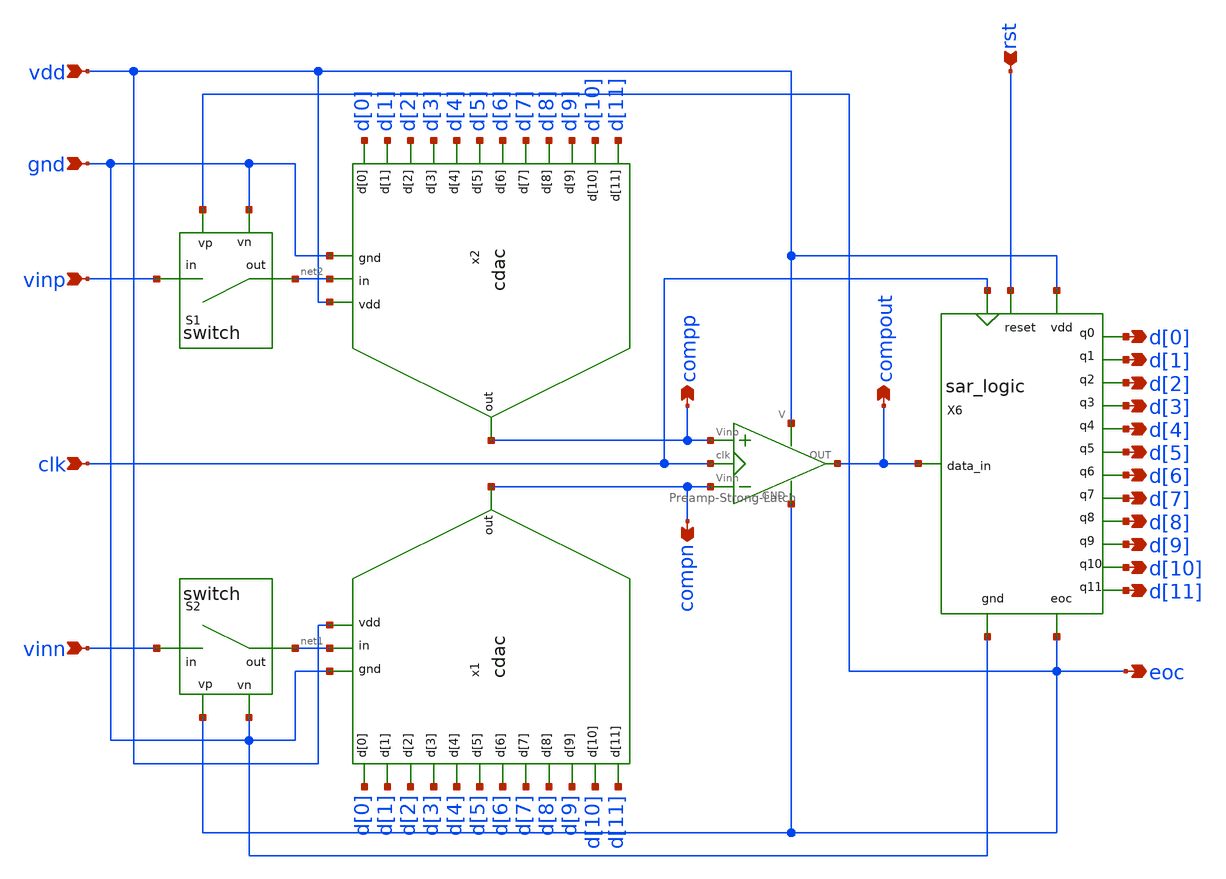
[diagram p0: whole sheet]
** sch_path: SAR_ADC/xschem/designs/sar_adc.sch
**.subckt sar_adc vinn vinp clk rst vdd gnd d[0] d[1] d[2] d[3] d[4] d[5] d[6] d[7] d[8] d[9] d[10]
*+ d[11] compp compn compout eoc
*.ipin vinn
*.ipin vinp
*.ipin clk
*.ipin rst
*.ipin vdd
*.ipin gnd
*.opin d[0]
*.opin d[1]
*.opin d[2]
*.opin d[3]
*.opin d[4]
*.opin d[5]
*.opin d[6]
*.opin d[7]
*.opin d[8]
*.opin d[9]
*.opin d[10]
*.opin d[11]
*.opin compp
*.opin compn
*.opin compout
*.opin eoc
x1 compn net1 d[9] d[7] d[0] d[11] d[3] d[4] d[2] d[1] d[8] d[6] d[5] d[10] gnd vdd cdac cu=5u
x2 compp net2 d[9] d[7] d[0] d[11] d[3] d[4] d[2] d[1] d[8] d[6] d[5] d[10] gnd vdd cdac cu=5u
X5 vdd compp compn compout clk eoc Preamp-Strong-Latch
X6 eoc vdd gnd clk compout d[0] d[10] d[11] d[1] d[2] d[3] d[4] d[5] d[6] d[7] d[8] d[9] rst
+ sar_logic
S1 vinp net2 eoc gnd swm1
S2 vinn net1 eoc gnd swm1
**.ends

* expanding   symbol:  cdac.sym # of pins=16
** sym_path: SAR_ADC/xschem/designs/cdac.sym
** sch_path: SAR_ADC/xschem/designs/cdac.sch
.subckt cdac out in d[9] d[7] d[0] d[11] d[3] d[4] d[2] d[1] d[8] d[6] d[5] d[10] gnd vdd  cu=5u
*.ipin d[0]
*.ipin d[1]
*.ipin d[2]
*.ipin d[3]
*.ipin d[4]
*.ipin d[5]
*.ipin d[6]
*.ipin d[7]
*.ipin d[8]
*.ipin d[9]
*.ipin d[10]
*.ipin d[11]
*.ipin vdd
*.ipin gnd
*.iopin out
*.iopin in
x1 in vdd gnd d[0] cdac_line CW={sqrt(2)*cu} CL={sqrt(2)*cu}
x2 in vdd gnd d[1] cdac_line CW={sqrt(3)*cu} CL={sqrt(3)*cu}
x3 in vdd gnd d[2] cdac_line CW={sqrt(4)*cu} CL={sqrt(4)*cu}
x4 in vdd gnd d[3] cdac_line CW={sqrt(8)*cu} CL={sqrt(8)*cu}
x5 in vdd gnd d[4] cdac_line CW={sqrt(16)*cu} CL={sqrt(16)*cu}
x6 in vdd gnd d[5] cdac_line CW={sqrt(32)*cu} CL={sqrt(32)*cu}
XCA out in cap_mim_1f5fF c_width={cu} c_length={cu} m=1
x7 out vdd gnd d[6] cdac_line CW={sqrt(1)*cu} CL={sqrt(1)*cu}
x8 out vdd gnd d[7] cdac_line CW={sqrt(2)*cu} CL={sqrt(2)*cu}
x9 out vdd gnd d[8] cdac_line CW={sqrt(4)*cu} CL={sqrt(4)*cu}
x10 out vdd gnd d[9] cdac_line CW={sqrt(8)*cu} CL={sqrt(8)*cu}
x11 out vdd gnd d[10] cdac_line CW={sqrt(16)*cu} CL={sqrt(16)*cu}
x12 out vdd gnd d[11] cdac_line CW={sqrt(32)*cu} CL={sqrt(32)*cu}
R1 out in 100T m=1
XC1 in gnd cap_mim_1f5fF c_width={cu} c_length={cu} m=1
.ends


* expanding   symbol:  Preamp-Strong-Latch.sym # of pins=6
** sym_path: SAR_ADC/xschem/designs/Preamp-Strong-Latch.sym
** sch_path: SAR_ADC/xschem/designs/Preamp-Strong-Latch.sch
.subckt Preamp-Strong-Latch V Vinp Vinn OUT clk GND
*.iopin V
*.iopin GND
*.iopin Vinp
*.iopin Vinn
*.iopin clk
*.iopin OUT
X1 net4 V GND net5 OUT net7 SR_nor
x2 V GND net4 net8 inv cl=0.28u wp=0.44u wn=0.22u wx=0.22u
x3 V GND net8 net3 inv cl=0.28u wp=0.44u wn=0.22u wx=0.22u
x4 V GND net5 net9 inv cl=0.28u wp=0.44u wn=0.22u wx=0.22u
x5 V GND net9 net6 inv cl=0.28u wp=0.44u wn=0.22u wx=0.22u
X6 V GND net2 net1 clk net3 net6 strongarm
X7 V GND Vinp clk net1 net2 Vinn preamp
.ends


* expanding   symbol:  cdac_line.sym # of pins=4
** sym_path: SAR_ADC/xschem/spice/cdac_line.sym
** sch_path: SAR_ADC/xschem/spice/cdac_line.sch
.subckt cdac_line vout vdd gnd vin  CW=1e-6 CL=1e-6
*.ipin vdd
*.ipin gnd
*.ipin vin
*.opin vout
x1 vdd gnd net1 net2 inv cl=0.28u wp=0.66u wn=0.22u
XC1 vout net1 cap_mim_2f0fF c_width=CW c_length=CL m=1
x2 vdd gnd net2 vin inv cl=0.28u wp=0.66u wn=0.22u
.ends


* expanding   symbol:  SR_nor.sym # of pins=6
** sym_path: SAR_ADC/xschem/designs/SR_nor.sym
** sch_path: SAR_ADC/xschem/designs/SR_nor.sch
.subckt SR_nor S V GND R Q Qn
*.iopin V
*.iopin GND
*.iopin S
*.iopin R
*.iopin Qn
*.iopin Q
X1 S Q Qn GND V norgate
X2 Qn R Q GND V norgate
.ends


* expanding   symbol:  inv.sym # of pins=4
** sym_path: SAR_ADC/xschem/designs/inv.sym
** sch_path: SAR_ADC/xschem/designs/inv.sch
.subckt inv vdd gnd vout vin  cl=0.28u wp=0.44u wn=0.22u wx=0.22u
*.ipin gnd
*.ipin vdd
*.ipin vin
*.opin vout
XM1 gnd vin vout gnd nfet_03v3 L=0.28u W=8u nf=1 ad='int((nf+1)/2) * W/nf * 0.18u' as='int((nf+2)/2) * W/nf * 0.18u'
+ pd='2*int((nf+1)/2) * (W/nf + 0.18u)' ps='2*int((nf+2)/2) * (W/nf + 0.18u)' nrd='0.18u / W' nrs='0.18u / W'
+ sa=0 sb=0 sd=0 m=1
XM2 vdd vin vout vdd pfet_03v3 L=0.28u W=8u nf=1 ad='int((nf+1)/2) * W/nf * 0.18u' as='int((nf+2)/2) * W/nf * 0.18u'
+ pd='2*int((nf+1)/2) * (W/nf + 0.18u)' ps='2*int((nf+2)/2) * (W/nf + 0.18u)' nrd='0.18u / W' nrs='0.18u / W'
+ sa=0 sb=0 sd=0 m=1
.ends


* expanding   symbol:  strongarm.sym # of pins=7
** sym_path: SAR_ADC/xschem/designs/strongarm.sym
** sch_path: SAR_ADC/xschem/designs/strongarm.sch
.subckt strongarm V GND Vin1 Vin2 CLK Vout1 Vout2
*.iopin V
*.iopin Vout1
*.iopin Vin1
*.iopin Vin2
*.iopin Vout2
*.iopin CLK
*.iopin GND
XM1 net3 Vout2 V V pfet_03v3 L=0.28u W=2u nf=1 ad='int((nf+1)/2) * W/nf * 0.18u' as='int((nf+2)/2) * W/nf * 0.18u'
+ pd='2*int((nf+1)/2) * (W/nf + 0.18u)' ps='2*int((nf+2)/2) * (W/nf + 0.18u)' nrd='0.18u / W' nrs='0.18u / W'
+ sa=0 sb=0 sd=0 m=1
XM2 Vout1 net1 GND GND nfet_03v3 L=0.28u W=2u nf=1 ad='int((nf+1)/2) * W/nf * 0.18u' as='int((nf+2)/2) * W/nf * 0.18u'
+ pd='2*int((nf+1)/2) * (W/nf + 0.18u)' ps='2*int((nf+2)/2) * (W/nf + 0.18u)' nrd='0.18u / W' nrs='0.18u / W'
+ sa=0 sb=0 sd=0 m=1
XM3 Vout2 Vout1 GND GND nfet_03v3 L=0.28u W=2u nf=1 ad='int((nf+1)/2) * W/nf * 0.18u' as='int((nf+2)/2) * W/nf * 0.18u'
+ pd='2*int((nf+1)/2) * (W/nf + 0.18u)' ps='2*int((nf+2)/2) * (W/nf + 0.18u)' nrd='0.18u / W' nrs='0.18u / W'
+ sa=0 sb=0 sd=0 m=1
XM4 Vout2 net1 GND GND nfet_03v3 L=0.28u W=2u nf=1 ad='int((nf+1)/2) * W/nf * 0.18u' as='int((nf+2)/2) * W/nf * 0.18u'
+ pd='2*int((nf+1)/2) * (W/nf + 0.18u)' ps='2*int((nf+2)/2) * (W/nf + 0.18u)' nrd='0.18u / W' nrs='0.18u / W'
+ sa=0 sb=0 sd=0 m=1
XM5 Vout1 Vout2 GND GND nfet_03v3 L=0.28u W=2u nf=1 ad='int((nf+1)/2) * W/nf * 0.18u' as='int((nf+2)/2) * W/nf * 0.18u'
+ pd='2*int((nf+1)/2) * (W/nf + 0.18u)' ps='2*int((nf+2)/2) * (W/nf + 0.18u)' nrd='0.18u / W' nrs='0.18u / W'
+ sa=0 sb=0 sd=0 m=1
XM6 net2 Vout1 V V pfet_03v3 L=0.28u W=2u nf=1 ad='int((nf+1)/2) * W/nf * 0.18u' as='int((nf+2)/2) * W/nf * 0.18u'
+ pd='2*int((nf+1)/2) * (W/nf + 0.18u)' ps='2*int((nf+2)/2) * (W/nf + 0.18u)' nrd='0.18u / W' nrs='0.18u / W'
+ sa=0 sb=0 sd=0 m=1
XM7 Vout1 Vin1 net3 V pfet_03v3 L=0.28u W=10u nf=1 ad='int((nf+1)/2) * W/nf * 0.18u' as='int((nf+2)/2) * W/nf * 0.18u'
+ pd='2*int((nf+1)/2) * (W/nf + 0.18u)' ps='2*int((nf+2)/2) * (W/nf + 0.18u)' nrd='0.18u / W' nrs='0.18u / W'
+ sa=0 sb=0 sd=0 m=1
XM8 Vout2 Vin2 net2 V pfet_03v3 L=0.28u W=10u nf=1 ad='int((nf+1)/2) * W/nf * 0.18u' as='int((nf+2)/2) * W/nf * 0.18u'
+ pd='2*int((nf+1)/2) * (W/nf + 0.18u)' ps='2*int((nf+2)/2) * (W/nf + 0.18u)' nrd='0.18u / W' nrs='0.18u / W'
+ sa=0 sb=0 sd=0 m=1
x1 V GND net4 CLK inv cl=0.28u wp=0.44u wn=0.22u wx=4u
x2 V GND net1 net4 inv cl=0.28u wp=0.44u wn=0.22u wx=4u
.ends


* expanding   symbol:  preamp.sym # of pins=7
** sym_path: SAR_ADC/xschem/designs/preamp.sym
** sch_path: SAR_ADC/xschem/designs/preamp.sch
.subckt preamp V GND Vin1 clk Vout1 Vout2 Vin2
*.iopin V
*.iopin GND
*.iopin Vout2
*.iopin Vout1
*.iopin clk
*.iopin Vin2
*.iopin Vin1
XM26 Vout2 clk GND GND nfet_03v3 L=.5u W=.22u nf=1 ad='int((nf+1)/2) * W/nf * 0.18u' as='int((nf+2)/2) * W/nf * 0.18u'
+ pd='2*int((nf+1)/2) * (W/nf + 0.18u)' ps='2*int((nf+2)/2) * (W/nf + 0.18u)' nrd='0.18u / W' nrs='0.18u / W'
+ sa=0 sb=0 sd=0 m=1
XM27 Vout1 clk GND GND nfet_03v3 L=.5u W=.22u nf=1 ad='int((nf+1)/2) * W/nf * 0.18u' as='int((nf+2)/2) * W/nf * 0.18u'
+ pd='2*int((nf+1)/2) * (W/nf + 0.18u)' ps='2*int((nf+2)/2) * (W/nf + 0.18u)' nrd='0.18u / W' nrs='0.18u / W'
+ sa=0 sb=0 sd=0 m=1
XM24 Vout1 Vin2 net1 V pfet_03v3 L=.28u W=8u nf=1 ad='int((nf+1)/2) * W/nf * 0.18u' as='int((nf+2)/2) * W/nf * 0.18u'
+ pd='2*int((nf+1)/2) * (W/nf + 0.18u)' ps='2*int((nf+2)/2) * (W/nf + 0.18u)' nrd='0.18u / W' nrs='0.18u / W'
+ sa=0 sb=0 sd=0 m=1
XM25 Vout2 Vin1 net1 V pfet_03v3 L=.28u W=8u nf=1 ad='int((nf+1)/2) * W/nf * 0.18u' as='int((nf+2)/2) * W/nf * 0.18u'
+ pd='2*int((nf+1)/2) * (W/nf + 0.18u)' ps='2*int((nf+2)/2) * (W/nf + 0.18u)' nrd='0.18u / W' nrs='0.18u / W'
+ sa=0 sb=0 sd=0 m=1
XM1 V clk net1 V pfet_03v3 L=2u W=1u nf=1 ad='int((nf+1)/2) * W/nf * 0.18u' as='int((nf+2)/2) * W/nf * 0.18u'
+ pd='2*int((nf+1)/2) * (W/nf + 0.18u)' ps='2*int((nf+2)/2) * (W/nf + 0.18u)' nrd='0.18u / W' nrs='0.18u / W'
+ sa=0 sb=0 sd=0 m=1
.ends


* expanding   symbol:  norgate.sym # of pins=5
** sym_path: SAR_ADC/xschem/designs/norgate.sym
** sch_path: SAR_ADC/xschem/designs/norgate.sch
.subckt norgate A B Z GND V
*.iopin GND
*.iopin A
*.iopin B
*.iopin V
*.iopin Z
XM3 V A net2 V pfet_03v3 L=0.28u W=0.22u nf=1 ad='int((nf+1)/2) * W/nf * 0.18u' as='int((nf+2)/2) * W/nf * 0.18u'
+ pd='2*int((nf+1)/2) * (W/nf + 0.18u)' ps='2*int((nf+2)/2) * (W/nf + 0.18u)' nrd='0.18u / W' nrs='0.18u / W'
+ sa=0 sb=0 sd=0 m=1
XM6 net2 B Z V pfet_03v3 L=0.28u W=0.22u nf=1 ad='int((nf+1)/2) * W/nf * 0.18u' as='int((nf+2)/2) * W/nf * 0.18u'
+ pd='2*int((nf+1)/2) * (W/nf + 0.18u)' ps='2*int((nf+2)/2) * (W/nf + 0.18u)' nrd='0.18u / W' nrs='0.18u / W'
+ sa=0 sb=0 sd=0 m=1
XM9 V B net1 V pfet_03v3 L=0.28u W=0.22u nf=1 ad='int((nf+1)/2) * W/nf * 0.18u' as='int((nf+2)/2) * W/nf * 0.18u'
+ pd='2*int((nf+1)/2) * (W/nf + 0.18u)' ps='2*int((nf+2)/2) * (W/nf + 0.18u)' nrd='0.18u / W' nrs='0.18u / W'
+ sa=0 sb=0 sd=0 m=1
XM12 net1 A Z V pfet_03v3 L=0.28u W=0.22u nf=1 ad='int((nf+1)/2) * W/nf * 0.18u' as='int((nf+2)/2) * W/nf * 0.18u'
+ pd='2*int((nf+1)/2) * (W/nf + 0.18u)' ps='2*int((nf+2)/2) * (W/nf + 0.18u)' nrd='0.18u / W' nrs='0.18u / W'
+ sa=0 sb=0 sd=0 m=1
XM2 Z B GND GND nfet_03v3 L=0.28u W=0.22u nf=1 ad='int((nf+1)/2) * W/nf * 0.18u' as='int((nf+2)/2) * W/nf * 0.18u'
+ pd='2*int((nf+1)/2) * (W/nf + 0.18u)' ps='2*int((nf+2)/2) * (W/nf + 0.18u)' nrd='0.18u / W' nrs='0.18u / W'
+ sa=0 sb=0 sd=0 m=1
XM4 Z A GND GND nfet_03v3 L=0.28u W=0.22u nf=1 ad='int((nf+1)/2) * W/nf * 0.18u' as='int((nf+2)/2) * W/nf * 0.18u'
+ pd='2*int((nf+1)/2) * (W/nf + 0.18u)' ps='2*int((nf+2)/2) * (W/nf + 0.18u)' nrd='0.18u / W' nrs='0.18u / W'
+ sa=0 sb=0 sd=0 m=1
.ends

.end
